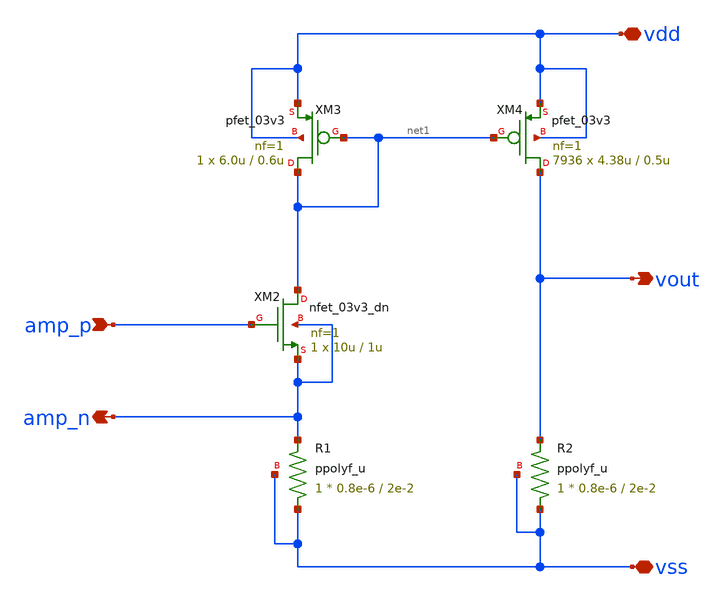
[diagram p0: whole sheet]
** sch_path: maple0705/SAR_ADC/xschem/ldo_currentmirror_lvs.sch
**.subckt ldo_currentmirror_lvs vdd vss vout amp_p amp_n
*.iopin vdd
*.iopin vss
*.opin vout
*.ipin amp_p
*.opin amp_n
XM3 net1 net1 vdd vdd pfet_03v3 L=0.6u W=6.0u nf=1 ad='int((nf+1)/2) * W/nf * 0.18u' as='int((nf+2)/2) * W/nf * 0.18u'
+ pd='2*int((nf+1)/2) * (W/nf + 0.18u)' ps='2*int((nf+2)/2) * (W/nf + 0.18u)' nrd='0.18u / W' nrs='0.18u / W'
+ sa=0 sb=0 sd=0 m=1
XM4 vout net1 vdd vdd pfet_03v3 L=0.5u W=4.38u nf=1 ad='int((nf+1)/2) * W/nf * 0.18u' as='int((nf+2)/2) * W/nf * 0.18u'
+ pd='2*int((nf+1)/2) * (W/nf + 0.18u)' ps='2*int((nf+2)/2) * (W/nf + 0.18u)' nrd='0.18u / W' nrs='0.18u / W'
+ sa=0 sb=0 sd=0 m=7936
XM2 net1 amp_p amp_n amp_n nfet_03v3_dn L=1u W=10u nf=1 ad='int((nf+1)/2) * W/nf * 0.18u' as='int((nf+2)/2) * W/nf * 0.18u'
+ pd='2*int((nf+1)/2) * (W/nf + 0.18u)' ps='2*int((nf+2)/2) * (W/nf + 0.18u)' nrd='0.18u / W' nrs='0.18u / W'
+ sa=0 sb=0 sd=0 m=1
R1 vss amp_n vss ppolyf_u W=0.8e-6 L=2e-2 m=1
R2 vss vout vss ppolyf_u W=0.8e-6 L=2e-2 m=1
**.ends
.end
